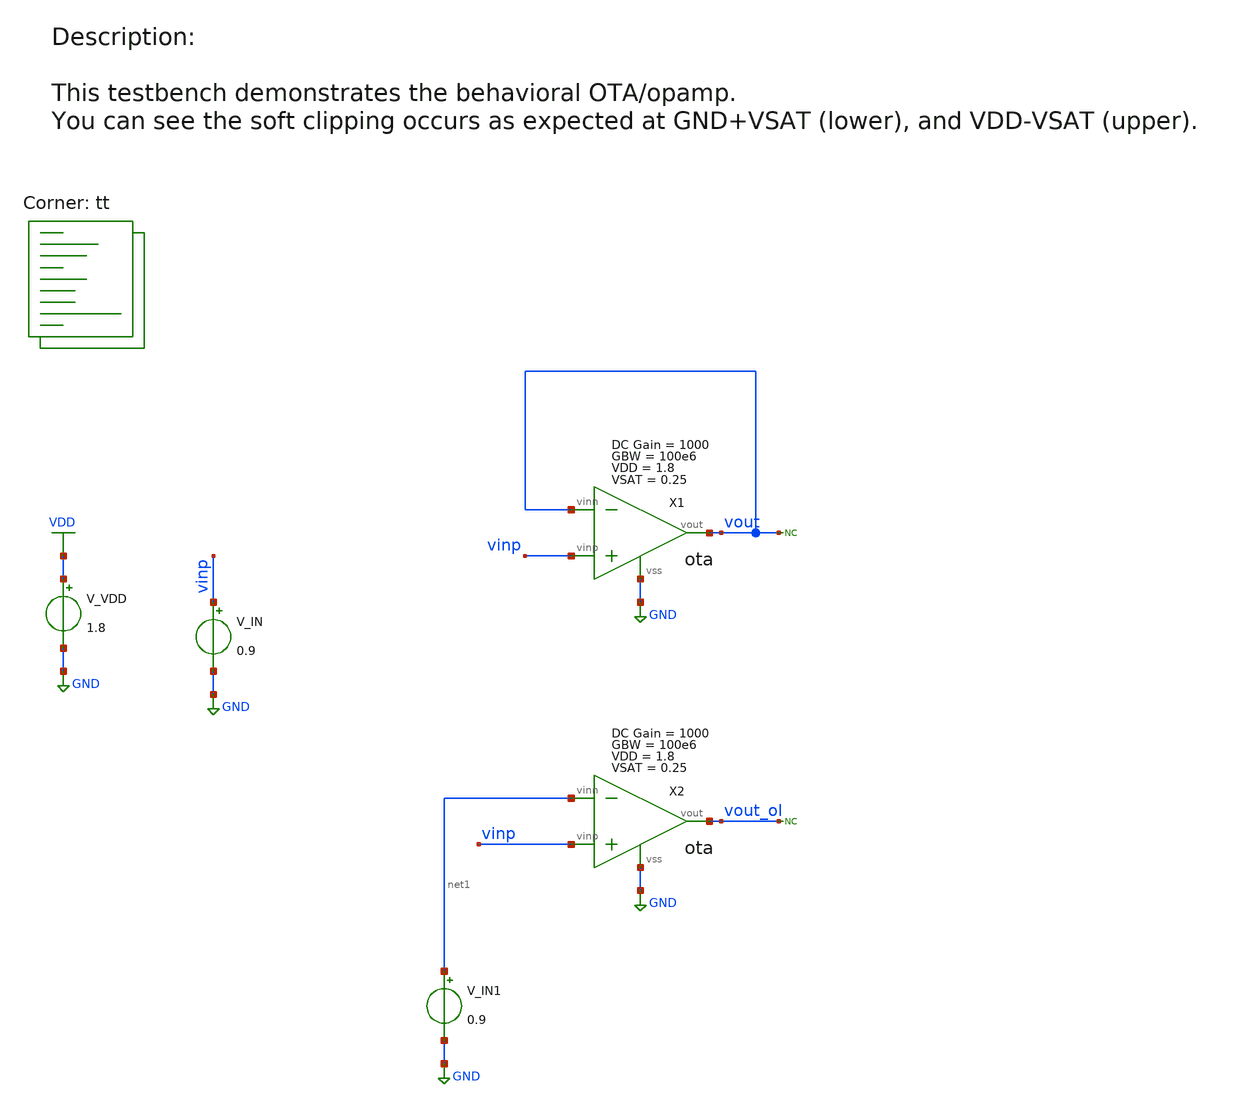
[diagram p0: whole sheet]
** sch_path: xsch/tb/tb_ota_1_DC_sweep.sch
**.subckt tb_ota_1_DC_sweep
V_VDD VDD GND 1.8
.save i(v_vdd)
V_IN vinp GND 0.9
.save i(v_in)
* noconn vout
X1 vinp vout GND vout ota Ao=1000 VDD=1.8 VSAT=0.25 GBW=100e6 Rout_ol=100
* noconn vout_ol
X2 vinp vout_ol GND net1 ota Ao=1000 VDD=1.8 VSAT=0.25 GBW=100e6 Rout_ol=100
V_IN1 net1 GND 0.9
.save i(v_in1)
**** begin user architecture code


.control
  save all
  dc V_IN 0 1.8 0.01
  *op
  plot v(vout) v(vinp)

.endc



.lib $::SKYWATER_MODELS/sky130.lib.spice tt
**** end user architecture code
**.ends

* expanding   symbol:  behavioral/ota.sym # of pins=4
** sym_path: xsch/behavioral/ota.sym
** sch_path: xsch/behavioral/ota.sch
.subckt ota vinp vout vss vinn  Ao=1000 VDD=1.8 VSAT=0.25 GBW=100e6 Rout_ol=100
*.ipin vinp
*.ipin vinn
*.opin vout
*.iopin vss
R1 vcvs1_out_filt vcvs1_out 10k m=1
C1 vcvs1_out_filt vss {Ao/2/3.14/GBW/10e3} m=1
Rout_ol vout vcvs2_out {Rout_ol} m=1
V1 vinp_int vinp 0
V2 vinn_int vinn 0
B2 vcvs1_out vss V = {VDD/2 + (VDD/2-VSAT)*(tanh(V(vinp_int, vinn_int)*Ao/(VDD/2-VSAT)))}
B1 vcvs2_out vss V = {V(vcvs1_out_filt, vss)*1}
.ends

.GLOBAL GND
.GLOBAL VDD
.end
